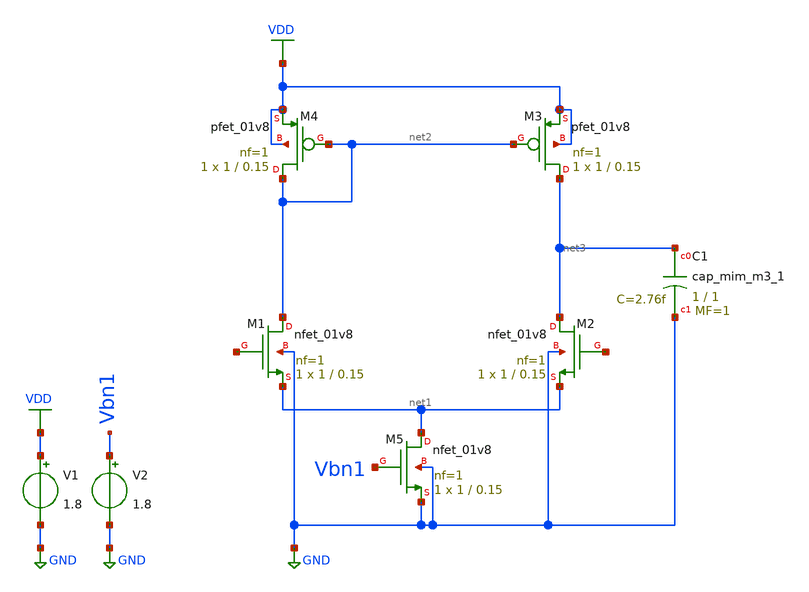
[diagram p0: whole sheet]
** sch_path: opamp_design/simple_one_stage_opamp/simple_one_stage_opamp.sch
**.subckt simple_one_stage_opamp
XM1 net2 net4 net1 GND sky130_fd_pr__nfet_01v8 L=0.15 W=1 nf=1 ad='int((nf+1)/2) * W/nf * 0.29' as='int((nf+2)/2) * W/nf * 0.29'
+ pd='2*int((nf+1)/2) * (W/nf + 0.29)' ps='2*int((nf+2)/2) * (W/nf + 0.29)' nrd='0.29 / W' nrs='0.29 / W'
+ sa=0 sb=0 sd=0 mult=1 m=1
XM4 net2 net2 VDD VDD sky130_fd_pr__pfet_01v8 L=0.15 W=1 nf=1 ad='int((nf+1)/2) * W/nf * 0.29' as='int((nf+2)/2) * W/nf * 0.29'
+ pd='2*int((nf+1)/2) * (W/nf + 0.29)' ps='2*int((nf+2)/2) * (W/nf + 0.29)' nrd='0.29 / W' nrs='0.29 / W'
+ sa=0 sb=0 sd=0 mult=1 m=1
XM2 net3 net5 net1 GND sky130_fd_pr__nfet_01v8 L=0.15 W=1 nf=1 ad='int((nf+1)/2) * W/nf * 0.29' as='int((nf+2)/2) * W/nf * 0.29'
+ pd='2*int((nf+1)/2) * (W/nf + 0.29)' ps='2*int((nf+2)/2) * (W/nf + 0.29)' nrd='0.29 / W' nrs='0.29 / W'
+ sa=0 sb=0 sd=0 mult=1 m=1
XM3 net3 net2 VDD VDD sky130_fd_pr__pfet_01v8 L=0.15 W=1 nf=1 ad='int((nf+1)/2) * W/nf * 0.29' as='int((nf+2)/2) * W/nf * 0.29'
+ pd='2*int((nf+1)/2) * (W/nf + 0.29)' ps='2*int((nf+2)/2) * (W/nf + 0.29)' nrd='0.29 / W' nrs='0.29 / W'
+ sa=0 sb=0 sd=0 mult=1 m=1
XM5 net1 Vbn1 GND GND sky130_fd_pr__nfet_01v8 L=0.15 W=1 nf=1 ad='int((nf+1)/2) * W/nf * 0.29' as='int((nf+2)/2) * W/nf * 0.29'
+ pd='2*int((nf+1)/2) * (W/nf + 0.29)' ps='2*int((nf+2)/2) * (W/nf + 0.29)' nrd='0.29 / W' nrs='0.29 / W'
+ sa=0 sb=0 sd=0 mult=1 m=1
V1 VDD GND 1.8
XC1 net3 GND sky130_fd_pr__cap_mim_m3_1 W=1 L=1 MF=1 m=1
V2 Vbn1 GND 1.8
**.ends
.GLOBAL GND
.GLOBAL VDD
.end
